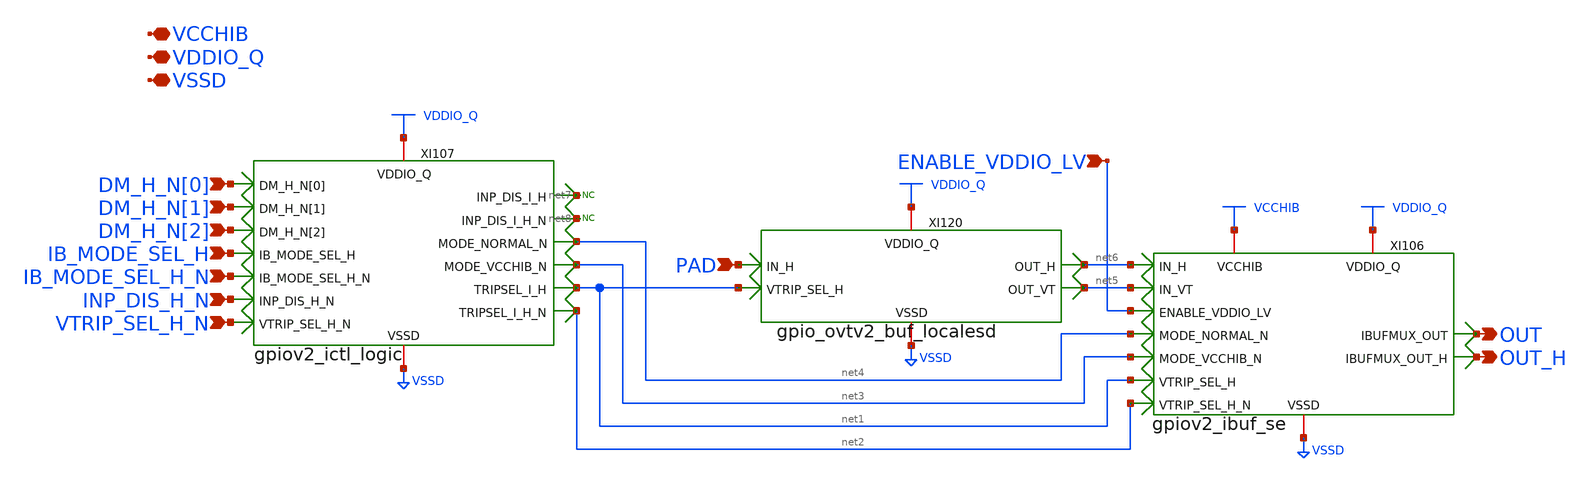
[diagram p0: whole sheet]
** sch_path: gpiov2_ipath.sch
* Copyright 2023 David Mitchell Bailey
* Licensed under the Apache License, Version 2.0 (the "License");
* you may not use this file except in compliance with the License.
* You may obtain a copy of the License at
* https://www.apache.org/licenses/LICENSE-2.0
* Unless required by applicable law or agreed to in writing, software
* distributed under the License is distributed on an "AS IS" BASIS,
* WITHOUT WARRANTIES OR CONDITIONS OF ANY KIND, either express or implied.
* See the License for the specific language governing permissions and
* limitations under the License.
**.subckt gpiov2_ipath PAD VCCHIB OUT DM_H_N[0] DM_H_N[1] DM_H_N[2] IB_MODE_SEL_H IB_MODE_SEL_H_N
*+ INP_DIS_H_N VTRIP_SEL_H_N OUT_H VDDIO_Q VSSD ENABLE_VDDIO_LV
*.ipin PAD
*.iopin VCCHIB
*.opin OUT
*.ipin DM_H_N[0]
*.ipin DM_H_N[1]
*.ipin DM_H_N[2]
*.ipin IB_MODE_SEL_H
*.ipin IB_MODE_SEL_H_N
*.ipin INP_DIS_H_N
*.ipin VTRIP_SEL_H_N
*.opin OUT_H
*.iopin VDDIO_Q
*.iopin VSSD
*.ipin ENABLE_VDDIO_LV
* noconn #net7
XI120 VDDIO_Q VSSD net1 PAD net5 net6 gpio_ovtv2_buf_localesd
XI107 VDDIO_Q VSSD VTRIP_SEL_H_N net7 DM_H_N[2] net8 DM_H_N[1] net2 DM_H_N[0] INP_DIS_H_N net1
+ IB_MODE_SEL_H_N net4 net3 IB_MODE_SEL_H gpiov2_ictl_logic
XI106 VCCHIB VDDIO_Q VSSD net4 OUT_H net1 net2 net6 ENABLE_VDDIO_LV OUT net3 net5 gpiov2_ibuf_se
* noconn #net8
**.ends
.end
